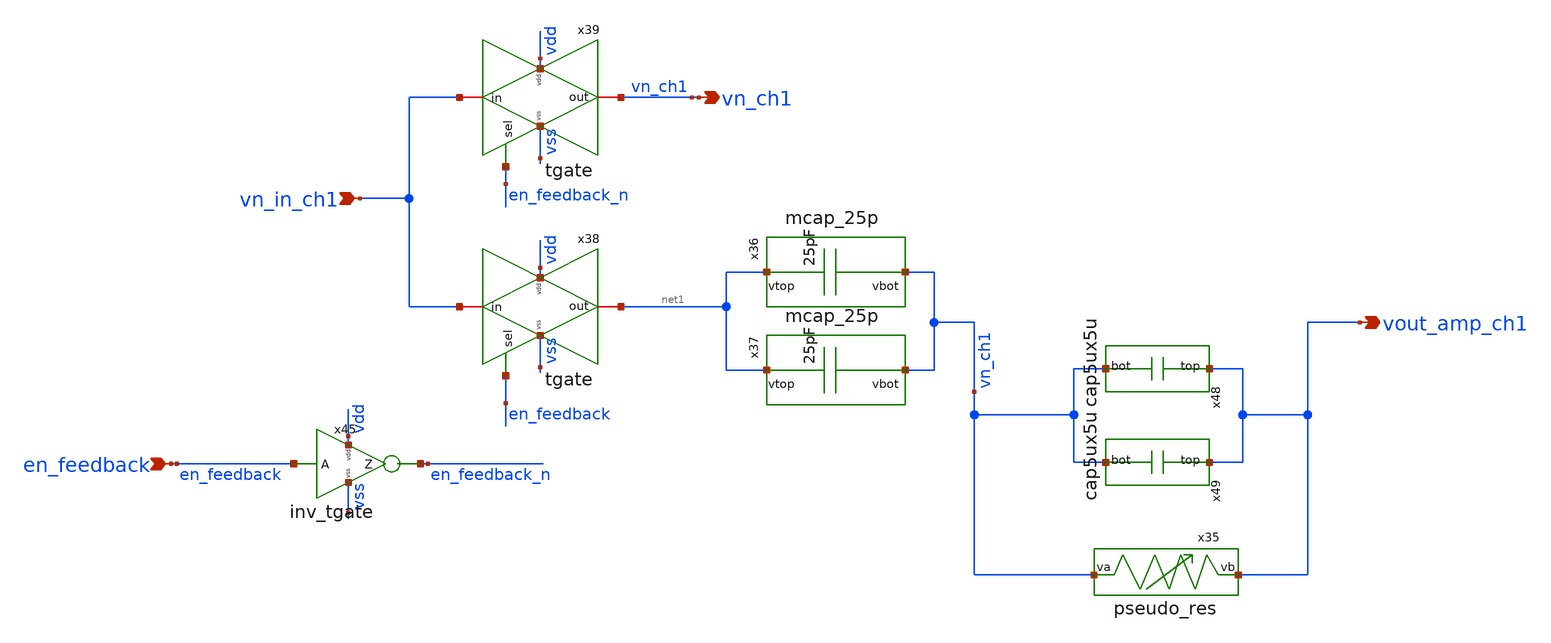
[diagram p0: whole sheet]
** sch_path: v2_feature_extr_withf/untitled-2.sch
**.subckt untitled-2 vn_in_ch1 en_feedback vn_ch1 vout_amp_ch1
*.ipin vn_in_ch1
*.ipin en_feedback
*.opin vn_ch1
*.opin vout_amp_ch1
x35 vout_amp_ch1 vn_ch1 pseudo_res
x36 net1 vn_ch1 mcap_25p
x37 net1 vn_ch1 mcap_25p
x38 vss vdd vn_in_ch1 net1 en_feedback tgate
x39 vss vdd vn_in_ch1 vn_ch1 en_feedback_n tgate
x45 vdd en_feedback en_feedback_n vss inv_tgate
x48 vout_amp_ch1 vn_ch1 cap5ux5u
x49 vout_amp_ch1 vn_ch1 cap5ux5u
**.ends
.end
